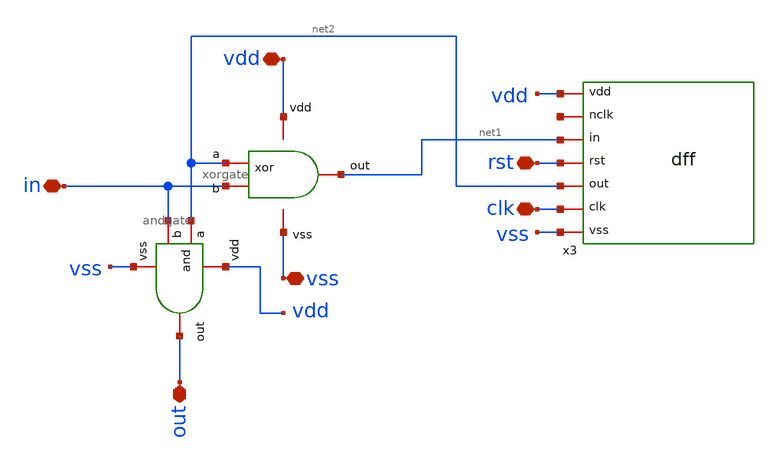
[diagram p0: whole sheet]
** sch_path: design/blocks/count1bit/schematic/count1bit.sch
**.subckt count1bit in clk out rst vss vdd
*.iopin in
*.iopin clk
*.iopin out
*.iopin rst
*.iopin vss
*.iopin vdd
x2 net2 vdd in vss net1 xorgate
x1 vdd net2 in out vss andgate
x3 vss clk net2 rst net1 net3 vdd dff
**.ends
.end
